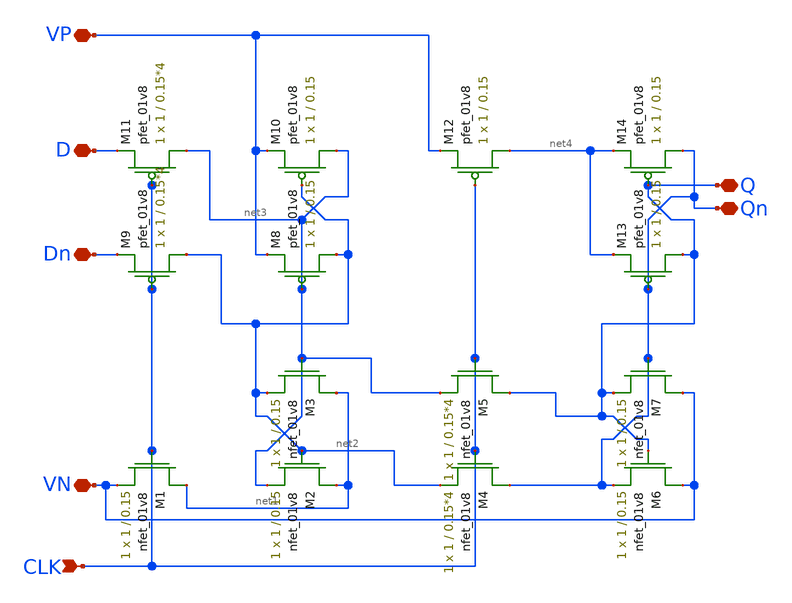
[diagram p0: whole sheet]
** sch_path: CSRL.sch
**.subckt CSRL CLK VN VP D Dn Q Qn
*.ipin CLK
*.iopin VN
*.iopin VP
*.iopin D
*.iopin Dn
*.iopin Q
*.iopin Qn
XM1 net1 CLK VN GND sky130_fd_pr__nfet_01v8 L=0.15 W=1 nf=1 ad='int((nf+1)/2) * W/nf * 0.29' as='int((nf+2)/2) * W/nf * 0.29'
+ pd='2*int((nf+1)/2) * (W/nf + 0.29)' ps='2*int((nf+2)/2) * (W/nf + 0.29)' nrd='0.29 / W' nrs='0.29 / W'
+ sa=0 sb=0 sd=0 mult=1 m=1
XM2 net1 net2 net3 GND sky130_fd_pr__nfet_01v8 L=0.15 W=1 nf=1 ad='int((nf+1)/2) * W/nf * 0.29' as='int((nf+2)/2) * W/nf * 0.29'
+ pd='2*int((nf+1)/2) * (W/nf + 0.29)' ps='2*int((nf+2)/2) * (W/nf + 0.29)' nrd='0.29 / W' nrs='0.29 / W'
+ sa=0 sb=0 sd=0 mult=1 m=1
XM3 net1 net3 net2 GND sky130_fd_pr__nfet_01v8 L=0.15 W=1 nf=1 ad='int((nf+1)/2) * W/nf * 0.29' as='int((nf+2)/2) * W/nf * 0.29'
+ pd='2*int((nf+1)/2) * (W/nf + 0.29)' ps='2*int((nf+2)/2) * (W/nf + 0.29)' nrd='0.29 / W' nrs='0.29 / W'
+ sa=0 sb=0 sd=0 mult=1 m=1
XM4 Qn CLK net2 GND sky130_fd_pr__nfet_01v8 L=0.15*4 W=1 nf=1 ad='int((nf+1)/2) * W/nf * 0.29' as='int((nf+2)/2) * W/nf * 0.29'
+ pd='2*int((nf+1)/2) * (W/nf + 0.29)' ps='2*int((nf+2)/2) * (W/nf + 0.29)' nrd='0.29 / W' nrs='0.29 / W'
+ sa=0 sb=0 sd=0 mult=1 m=1
XM5 Q CLK net3 GND sky130_fd_pr__nfet_01v8 L=0.15*4 W=1 nf=1 ad='int((nf+1)/2) * W/nf * 0.29' as='int((nf+2)/2) * W/nf * 0.29'
+ pd='2*int((nf+1)/2) * (W/nf + 0.29)' ps='2*int((nf+2)/2) * (W/nf + 0.29)' nrd='0.29 / W' nrs='0.29 / W'
+ sa=0 sb=0 sd=0 mult=1 m=1
XM6 VN Q Qn GND sky130_fd_pr__nfet_01v8 L=0.15 W=1 nf=1 ad='int((nf+1)/2) * W/nf * 0.29' as='int((nf+2)/2) * W/nf * 0.29'
+ pd='2*int((nf+1)/2) * (W/nf + 0.29)' ps='2*int((nf+2)/2) * (W/nf + 0.29)' nrd='0.29 / W' nrs='0.29 / W'
+ sa=0 sb=0 sd=0 mult=1 m=1
XM7 VN Qn Q GND sky130_fd_pr__nfet_01v8 L=0.15 W=1 nf=1 ad='int((nf+1)/2) * W/nf * 0.29' as='int((nf+2)/2) * W/nf * 0.29'
+ pd='2*int((nf+1)/2) * (W/nf + 0.29)' ps='2*int((nf+2)/2) * (W/nf + 0.29)' nrd='0.29 / W' nrs='0.29 / W'
+ sa=0 sb=0 sd=0 mult=1 m=1
XM8 net2 net3 VP VDD sky130_fd_pr__pfet_01v8 L=0.15 W=1 nf=1 ad='int((nf+1)/2) * W/nf * 0.29' as='int((nf+2)/2) * W/nf * 0.29'
+ pd='2*int((nf+1)/2) * (W/nf + 0.29)' ps='2*int((nf+2)/2) * (W/nf + 0.29)' nrd='0.29 / W' nrs='0.29 / W'
+ sa=0 sb=0 sd=0 mult=1 m=1
XM9 net2 CLK Dn VDD sky130_fd_pr__pfet_01v8 L=0.15*4 W=1 nf=1 ad='int((nf+1)/2) * W/nf * 0.29' as='int((nf+2)/2) * W/nf * 0.29'
+ pd='2*int((nf+1)/2) * (W/nf + 0.29)' ps='2*int((nf+2)/2) * (W/nf + 0.29)' nrd='0.29 / W' nrs='0.29 / W'
+ sa=0 sb=0 sd=0 mult=1 m=1
XM10 net3 net2 VP VDD sky130_fd_pr__pfet_01v8 L=0.15 W=1 nf=1 ad='int((nf+1)/2) * W/nf * 0.29' as='int((nf+2)/2) * W/nf * 0.29'
+ pd='2*int((nf+1)/2) * (W/nf + 0.29)' ps='2*int((nf+2)/2) * (W/nf + 0.29)' nrd='0.29 / W' nrs='0.29 / W'
+ sa=0 sb=0 sd=0 mult=1 m=1
XM11 net3 CLK D VDD sky130_fd_pr__pfet_01v8 L=0.15*4 W=1 nf=1 ad='int((nf+1)/2) * W/nf * 0.29' as='int((nf+2)/2) * W/nf * 0.29'
+ pd='2*int((nf+1)/2) * (W/nf + 0.29)' ps='2*int((nf+2)/2) * (W/nf + 0.29)' nrd='0.29 / W' nrs='0.29 / W'
+ sa=0 sb=0 sd=0 mult=1 m=1
XM12 net4 CLK VP VDD sky130_fd_pr__pfet_01v8 L=0.15 W=1 nf=1 ad='int((nf+1)/2) * W/nf * 0.29' as='int((nf+2)/2) * W/nf * 0.29'
+ pd='2*int((nf+1)/2) * (W/nf + 0.29)' ps='2*int((nf+2)/2) * (W/nf + 0.29)' nrd='0.29 / W' nrs='0.29 / W'
+ sa=0 sb=0 sd=0 mult=1 m=1
XM13 Q Qn net4 VDD sky130_fd_pr__pfet_01v8 L=0.15 W=1 nf=1 ad='int((nf+1)/2) * W/nf * 0.29' as='int((nf+2)/2) * W/nf * 0.29'
+ pd='2*int((nf+1)/2) * (W/nf + 0.29)' ps='2*int((nf+2)/2) * (W/nf + 0.29)' nrd='0.29 / W' nrs='0.29 / W'
+ sa=0 sb=0 sd=0 mult=1 m=1
XM14 Qn Q net4 VDD sky130_fd_pr__pfet_01v8 L=0.15 W=1 nf=1 ad='int((nf+1)/2) * W/nf * 0.29' as='int((nf+2)/2) * W/nf * 0.29'
+ pd='2*int((nf+1)/2) * (W/nf + 0.29)' ps='2*int((nf+2)/2) * (W/nf + 0.29)' nrd='0.29 / W' nrs='0.29 / W'
+ sa=0 sb=0 sd=0 mult=1 m=1
**.ends
.end
